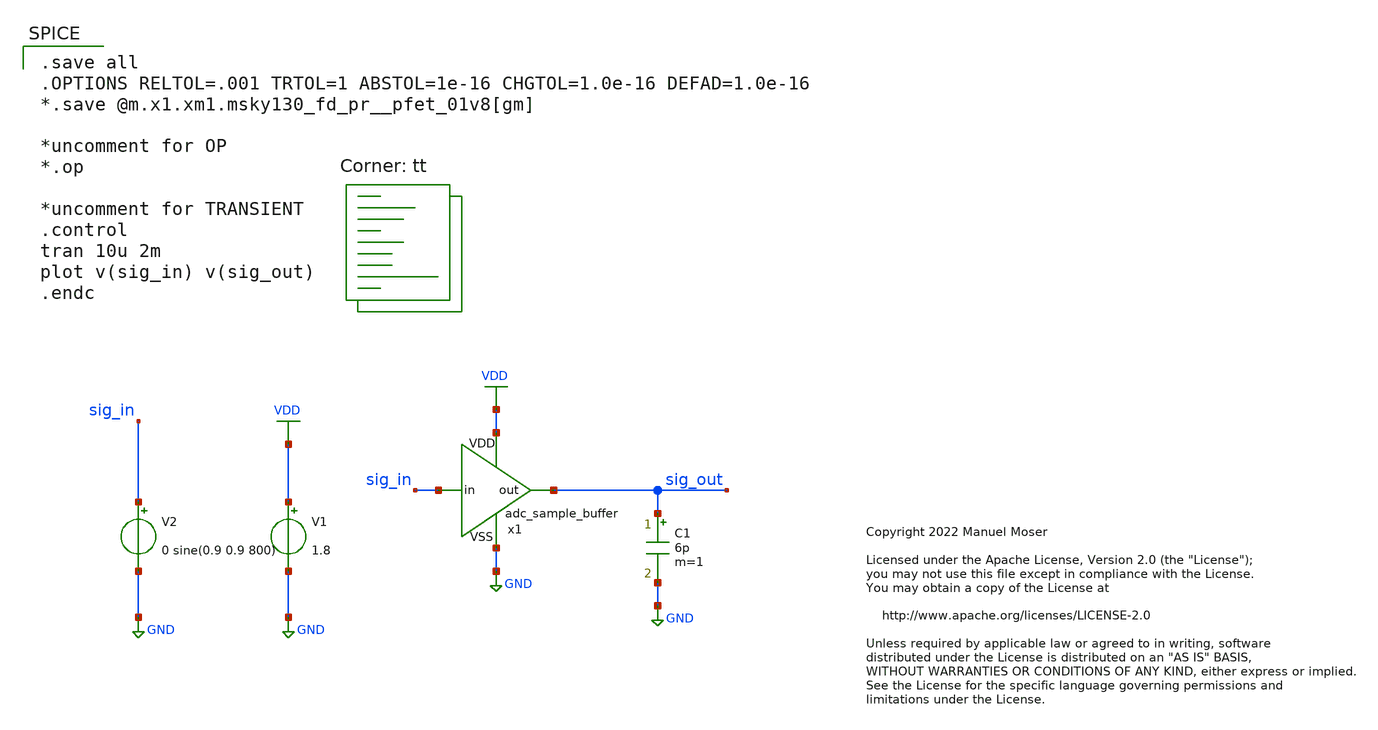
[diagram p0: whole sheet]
** sch_path: xschem/adc_sample_buffer/adc_sample_buffer_tb.sch
* Copyright 2022 Manuel Moser
* Licensed under the Apache License, Version 2.0 (the "License");
**.subckt adc_sample_buffer_tb
V1 VDD GND 1.8
V2 sig_in GND 0 sine(0.9 0.9 800)
C1 sig_out GND 6p m=1
x1 VDD sig_in sig_out GND adc_sample_buffer
**** begin user architecture code

.save all
.OPTIONS RELTOL=.001 TRTOL=1 ABSTOL=1e-16 CHGTOL=1.0e-16 DEFAD=1.0e-16
*.save @m.x1.xm1.msky130_fd_pr__pfet_01v8[gm]

*uncomment for OP
*.op

*uncomment for TRANSIENT
.control
tran 10u 2m
plot v(sig_in) v(sig_out)
.endc


.lib $::SKYWATER_MODELS/sky130.lib.spice tt
**** end user architecture code
**.ends
.GLOBAL GND
.GLOBAL VDD
.end
